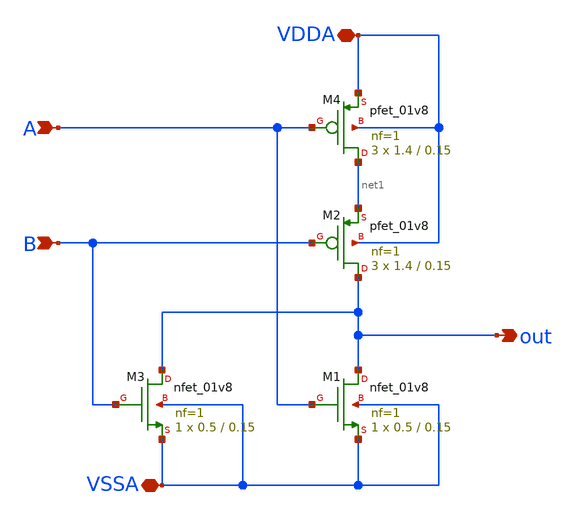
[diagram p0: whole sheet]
** sch_path: Xschem/sky130A/gate_nor_x1.sch
**.subckt gate_nor_x1 VDDA VSSA out A B
*.iopin VDDA
*.iopin VSSA
*.opin out
*.ipin A
*.ipin B
XM1 out A VSSA VSSA sky130_fd_pr__nfet_01v8 L=0.15 W=0.5 nf=1 ad='int((1 + 1)/2) * 0.5 / 1 * 0.29' as='int((1 + 2)/2) * 0.5 / 1 * 0.29'
+ pd='2*int((1 + 1)/2) * (0.5 / 1 + 0.29)' ps='2*int((1 + 2)/2) * (0.5 / 1 + 0.29)' nrd='0.29 / 0.5 ' nrs='0.29 / 0.5 '
+ sa=0 sb=0 sd=0 mult=1 m=1
XM2 out B net1 VDDA sky130_fd_pr__pfet_01v8 L=0.15 W=1.4 nf=1 ad='int((1 + 1)/2) * 1.4 / 1 * 0.29' as='int((1 + 2)/2) * 1.4 / 1 * 0.29'
+ pd='2*int((1 + 1)/2) * (1.4 / 1 + 0.29)' ps='2*int((1 + 2)/2) * (1.4 / 1 + 0.29)' nrd='0.29 / 1.4 ' nrs='0.29 / 1.4 '
+ sa=0 sb=0 sd=0 mult=3 m=3
XM3 out B VSSA VSSA sky130_fd_pr__nfet_01v8 L=0.15 W=0.5 nf=1 ad='int((1 + 1)/2) * 0.5 / 1 * 0.29' as='int((1 + 2)/2) * 0.5 / 1 * 0.29'
+ pd='2*int((1 + 1)/2) * (0.5 / 1 + 0.29)' ps='2*int((1 + 2)/2) * (0.5 / 1 + 0.29)' nrd='0.29 / 0.5 ' nrs='0.29 / 0.5 '
+ sa=0 sb=0 sd=0 mult=1 m=1
XM4 net1 A VDDA VDDA sky130_fd_pr__pfet_01v8 L=0.15 W=1.4 nf=1 ad='int((1 + 1)/2) * 1.4 / 1 * 0.29' as='int((1 + 2)/2) * 1.4 / 1 * 0.29'
+ pd='2*int((1 + 1)/2) * (1.4 / 1 + 0.29)' ps='2*int((1 + 2)/2) * (1.4 / 1 + 0.29)' nrd='0.29 / 1.4 ' nrs='0.29 / 1.4 '
+ sa=0 sb=0 sd=0 mult=3 m=3
**.ends
.end
